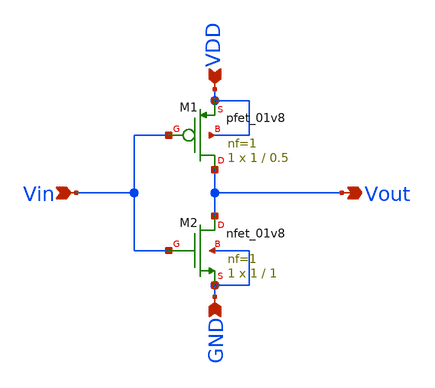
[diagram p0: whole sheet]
** sch_path: xschem/Inverter.sch
**.subckt Inverter Vout Vin VDD GND
*.opin Vout
*.ipin Vin
*.ipin VDD
*.ipin GND
XM1 Vout Vin VDD VDD sky130_fd_pr__pfet_01v8 L=0.5 W=1 nf=1 ad='int((nf+1)/2) * W/nf * 0.29' as='int((nf+2)/2) * W/nf * 0.29'
+ pd='2*int((nf+1)/2) * (W/nf + 0.29)' ps='2*int((nf+2)/2) * (W/nf + 0.29)' nrd='0.29 / W' nrs='0.29 / W'
+ sa=0 sb=0 sd=0 mult=1 m=1
XM2 Vout Vin GND GND sky130_fd_pr__nfet_01v8 L=1 W=1 nf=1 ad='int((nf+1)/2) * W/nf * 0.29' as='int((nf+2)/2) * W/nf * 0.29'
+ pd='2*int((nf+1)/2) * (W/nf + 0.29)' ps='2*int((nf+2)/2) * (W/nf + 0.29)' nrd='0.29 / W' nrs='0.29 / W'
+ sa=0 sb=0 sd=0 mult=1 m=1
**.ends
.end
